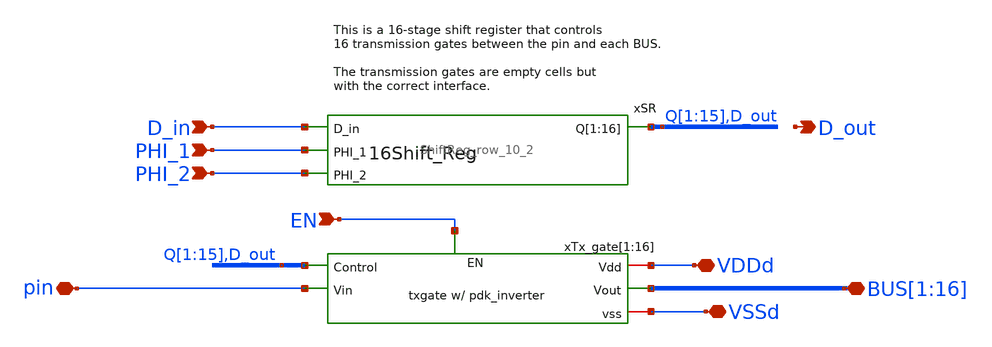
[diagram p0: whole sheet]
** sch_path: designs/libs/core_swmatrix/swmatrix_row_10.sch
**.subckt swmatrix_row_10 pin PHI_2 PHI_1
*+ BUS[1],BUS[2],BUS[3],BUS[4],BUS[5],BUS[6],BUS[7],BUS[8],BUS[9],BUS[10],BUS[11],BUS[12],BUS[13],BUS[14],BUS[15],BUS[16] D_in D_out VDDd VSSd EN
*.iopin pin
*.ipin PHI_2
*.ipin PHI_1
*.iopin
*+ BUS[1],BUS[2],BUS[3],BUS[4],BUS[5],BUS[6],BUS[7],BUS[8],BUS[9],BUS[10],BUS[11],BUS[12],BUS[13],BUS[14],BUS[15],BUS[16]
*.ipin D_in
*.opin D_out
*.iopin VDDd
*.iopin VSSd
*.ipin EN
xSR Q[1] Q[2] Q[3] Q[4] Q[5] Q[6] Q[7] Q[8] Q[9] Q[10] Q[11] Q[12] Q[13] Q[14] Q[15] D_out D_in
+ PHI_1 PHI_2 ShiftReg_row_10_2
xTx_gate[1] VDDd Q[1] BUS[1] pin VSSd EN transmission_gate_2
xTx_gate[2] VDDd Q[2] BUS[2] pin VSSd EN transmission_gate_2
xTx_gate[3] VDDd Q[3] BUS[3] pin VSSd EN transmission_gate_2
xTx_gate[4] VDDd Q[4] BUS[4] pin VSSd EN transmission_gate_2
xTx_gate[5] VDDd Q[5] BUS[5] pin VSSd EN transmission_gate_2
xTx_gate[6] VDDd Q[6] BUS[6] pin VSSd EN transmission_gate_2
xTx_gate[7] VDDd Q[7] BUS[7] pin VSSd EN transmission_gate_2
xTx_gate[8] VDDd Q[8] BUS[8] pin VSSd EN transmission_gate_2
xTx_gate[9] VDDd Q[9] BUS[9] pin VSSd EN transmission_gate_2
xTx_gate[10] VDDd Q[10] BUS[10] pin VSSd EN transmission_gate_2
xTx_gate[11] VDDd Q[11] BUS[11] pin VSSd EN transmission_gate_2
xTx_gate[12] VDDd Q[12] BUS[12] pin VSSd EN transmission_gate_2
xTx_gate[13] VDDd Q[13] BUS[13] pin VSSd EN transmission_gate_2
xTx_gate[14] VDDd Q[14] BUS[14] pin VSSd EN transmission_gate_2
xTx_gate[15] VDDd Q[15] BUS[15] pin VSSd EN transmission_gate_2
xTx_gate[16] VDDd D_out BUS[16] pin VSSd EN transmission_gate_2
**.ends
.end
